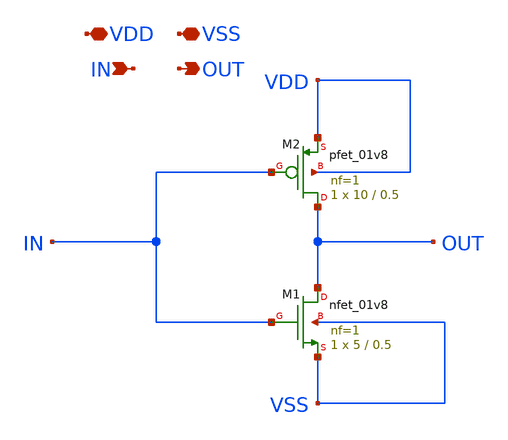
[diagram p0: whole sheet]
** sch_path: Xschem/TOP/INV_1.sch
**.subckt INV_1 VDD VSS IN OUT
*.iopin VDD
*.iopin VSS
*.ipin IN
*.opin OUT
XM1 OUT IN VSS VSS sky130_fd_pr__nfet_01v8 L=0.5 W=5 nf=1 ad='int((nf+1)/2) * W/nf * 0.29' as='int((nf+2)/2) * W/nf * 0.29'
+ pd='2*int((nf+1)/2) * (W/nf + 0.29)' ps='2*int((nf+2)/2) * (W/nf + 0.29)' nrd='0.29 / W' nrs='0.29 / W'
+ sa=0 sb=0 sd=0 mult=1 m=1
XM2 OUT IN VDD VDD sky130_fd_pr__pfet_01v8 L=0.5 W=10 nf=1 ad='int((nf+1)/2) * W/nf * 0.29' as='int((nf+2)/2) * W/nf * 0.29'
+ pd='2*int((nf+1)/2) * (W/nf + 0.29)' ps='2*int((nf+2)/2) * (W/nf + 0.29)' nrd='0.29 / W' nrs='0.29 / W'
+ sa=0 sb=0 sd=0 mult=1 m=1
**.ends
.end
